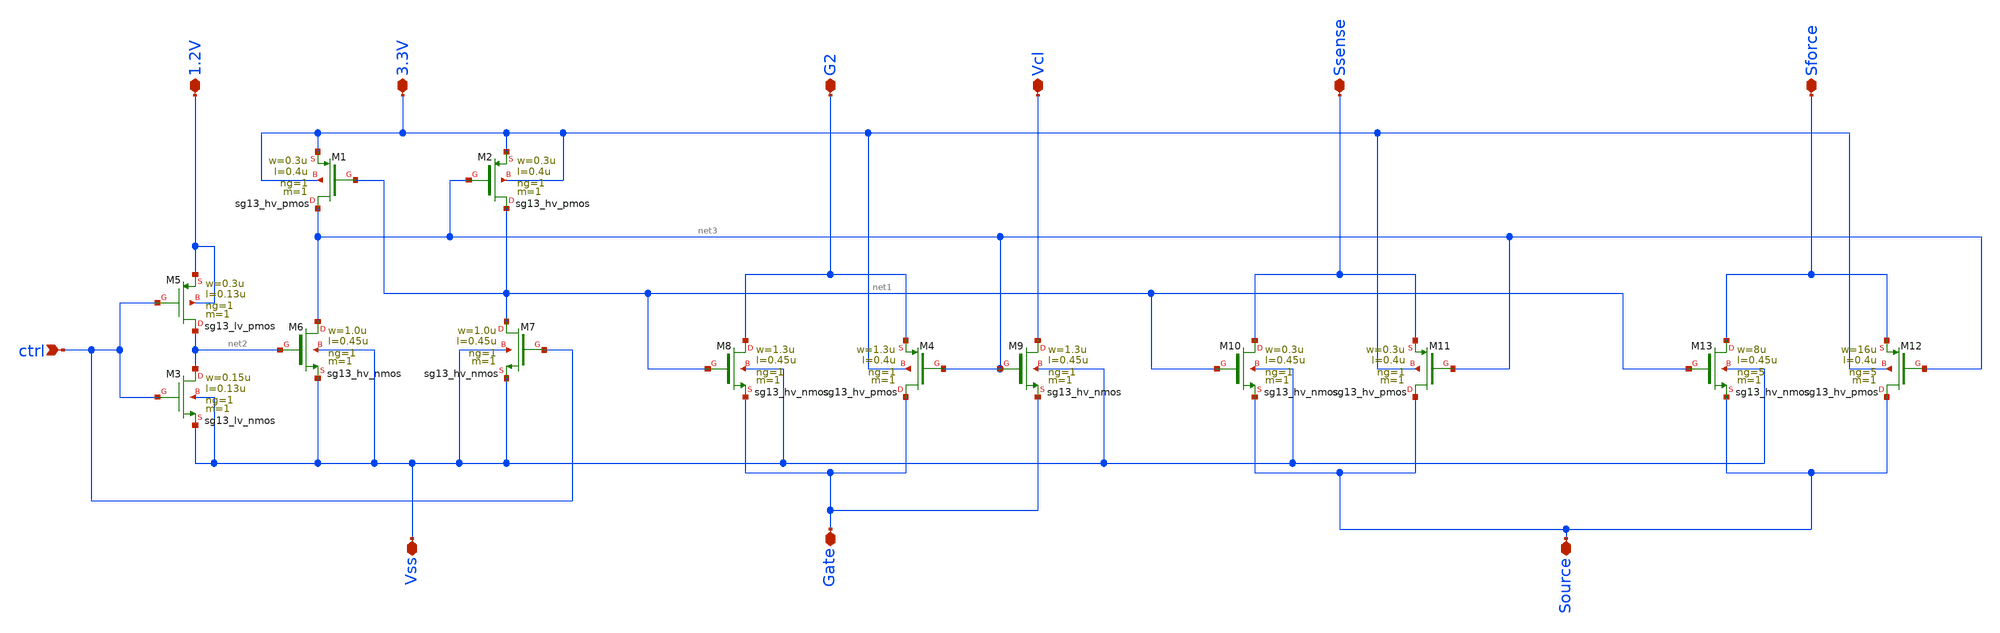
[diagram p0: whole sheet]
** sch_path: design_data/xschem/level_shifter_hor.sch
* Copyright 2025 IHP PDK Authors
**.subckt level_shifter_hor Gate Vss G2 3.3V ctrl 1.2V Vcl Ssense Source Sforce
*.iopin Gate
*.iopin Vss
*.iopin G2
*.iopin 3.3V
*.ipin ctrl
*.iopin 1.2V
*.iopin Vcl
*.iopin Ssense
*.iopin Source
*.iopin Sforce
XM2 net1 net3 3.3V 3.3V sg13_hv_pmos w=0.3u l=0.4u ng=1 m=1 mm_ok=1
XM3 net2 ctrl Vss Vss sg13_lv_nmos w=0.15u l=0.13u ng=1 m=1 mm_ok=1
XM5 net2 ctrl 1.2V 1.2V sg13_lv_pmos w=0.3u l=0.13u ng=1 m=1 mm_ok=1
XM1 net3 net1 3.3V 3.3V sg13_hv_pmos w=0.3u l=0.4u ng=1 m=1 mm_ok=1
XM4 Gate net3 G2 3.3V sg13_hv_pmos w=1.3u l=0.4u ng=1 m=1 mm_ok=1
XM8 G2 net1 Gate Vss sg13_hv_nmos w=1.3u l=0.45u ng=1 m=1 mm_ok=1
XM6 net3 net2 Vss Vss sg13_hv_nmos w=1.0u l=0.45u ng=1 m=1 mm_ok=1
XM7 net1 ctrl Vss Vss sg13_hv_nmos w=1.0u l=0.45u ng=1 m=1 mm_ok=1
XM9 Vcl net3 Gate Vss sg13_hv_nmos w=1.3u l=0.45u ng=1 m=1 mm_ok=1
XM12 Source net3 Sforce 3.3V sg13_hv_pmos w=16u l=0.4u ng=5 m=1 mm_ok=1
XM13 Sforce net1 Source Vss sg13_hv_nmos w=8u l=0.45u ng=5 m=1 mm_ok=1
XM10 Ssense net1 Source Vss sg13_hv_nmos w=0.3u l=0.45u ng=1 m=1 mm_ok=1
XM11 Source net3 Ssense 3.3V sg13_hv_pmos w=0.3u l=0.4u ng=1 m=1 mm_ok=1
**.ends
.end
